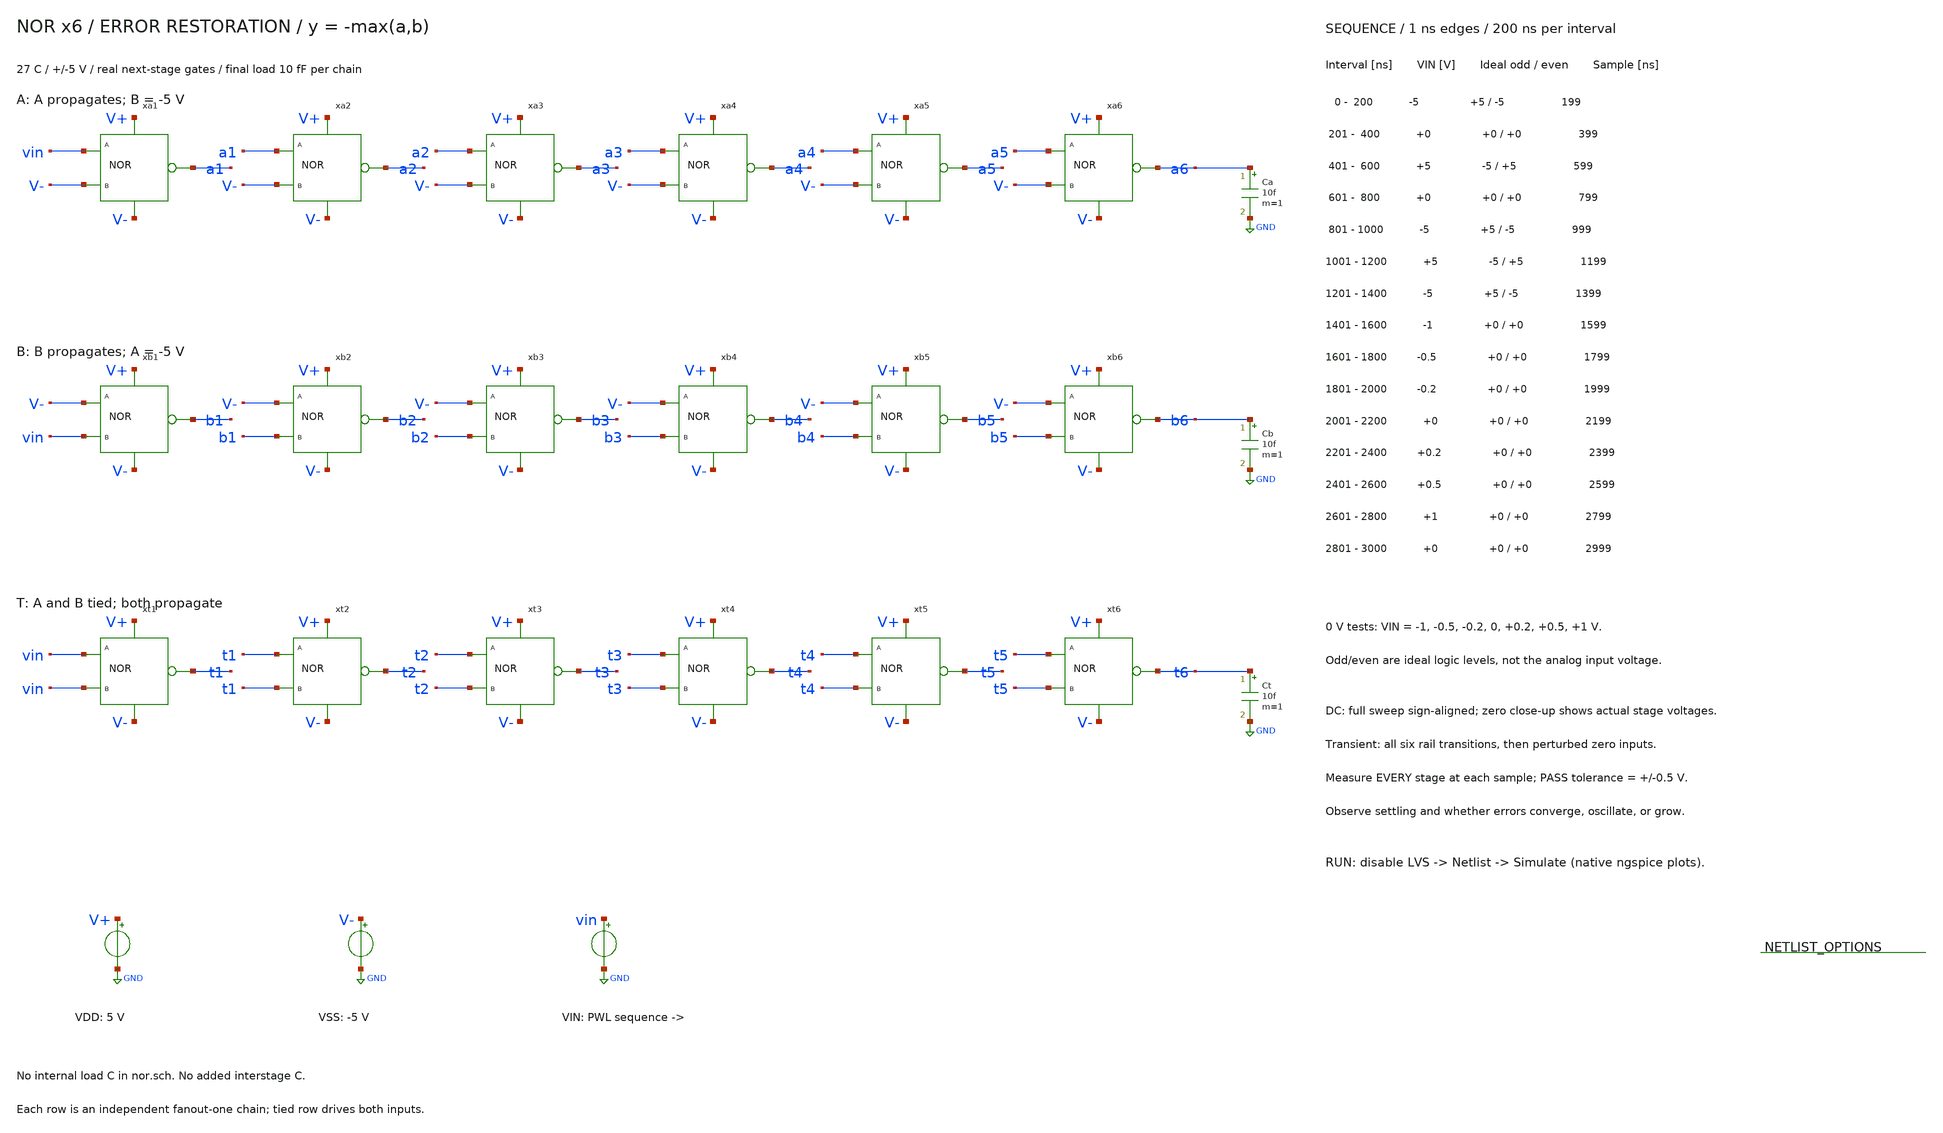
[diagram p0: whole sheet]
** sch_path: member_project/balanced-ternary-logic/PenguinEino/nor_chain_tb.sch
**.subckt nor_chain_tb
xa1 vin V- a1 V+ V- nor
xa2 a1 V- a2 V+ V- nor
xa3 a2 V- a3 V+ V- nor
xa4 a3 V- a4 V+ V- nor
xa5 a4 V- a5 V+ V- nor
xa6 a5 V- a6 V+ V- nor
Ca a6 GND 10f m=1
xb1 V- vin b1 V+ V- nor
xb2 V- b1 b2 V+ V- nor
xb3 V- b2 b3 V+ V- nor
xb4 V- b3 b4 V+ V- nor
xb5 V- b4 b5 V+ V- nor
xb6 V- b5 b6 V+ V- nor
Cb b6 GND 10f m=1
xt1 vin vin t1 V+ V- nor
xt2 t1 t1 t2 V+ V- nor
xt3 t2 t2 t3 V+ V- nor
xt4 t3 t3 t4 V+ V- nor
xt5 t4 t4 t5 V+ V- nor
xt6 t5 t5 t6 V+ V- nor
Ct t6 GND 10f m=1
VDD V+ GND 5
VSS V- GND -5
VIN vin GND PWL(0 -5 200n -5 201n 0 400n 0 401n 5 600n 5 601n 0 800n 0 801n -5 1000n -5 1001n 5
+ 1200n 5 1201n -5 1400n -5 1401n -1 1600n -1 1601n -0.5 1800n -0.5 1801n -0.2 2000n -0.2 2001n 0 2200n 0
+ 2201n 0.2 2400n 0.2 2401n 0.5 2600n 0.5 2601n 1 2800n 1 2801n 0 3000n 0)
**** begin user architecture code
 .include $::LIB/ip62_models

.temp 27
.options rshunt=1e12
.control
save all
set wr_singlescale
set wr_vecnames
setplot const
let failures=0
dc VIN -5 5 0.025
let as1=-v(a1)
let as2=v(a2)
let as3=-v(a3)
let as4=v(a4)
let as5=-v(a5)
let as6=v(a6)
plot v(vin) as1 as2 as3 as4 as5 as6 ylimit -5.5 5.5 title 'NOR a: DC sign-aligned stages'
plot v(vin) v(a1) v(a2) v(a3) v(a4) v(a5) v(a6) xlimit -1 1 ylimit -0.7 0.7 title 'NOR a: zero restoration actual voltages'
let bs1=-v(b1)
let bs2=v(b2)
let bs3=-v(b3)
let bs4=v(b4)
let bs5=-v(b5)
let bs6=v(b6)
plot v(vin) bs1 bs2 bs3 bs4 bs5 bs6 ylimit -5.5 5.5 title 'NOR b: DC sign-aligned stages'
plot v(vin) v(b1) v(b2) v(b3) v(b4) v(b5) v(b6) xlimit -1 1 ylimit -0.7 0.7 title 'NOR b: zero restoration actual voltages'
let ts1=-v(t1)
let ts2=v(t2)
let ts3=-v(t3)
let ts4=v(t4)
let ts5=-v(t5)
let ts6=v(t6)
plot v(vin) ts1 ts2 ts3 ts4 ts5 ts6 ylimit -5.5 5.5 title 'NOR t: DC sign-aligned stages'
plot v(vin) v(t1) v(t2) v(t3) v(t4) v(t5) v(t6) xlimit -1 1 ylimit -0.7 0.7 title 'NOR t: zero restoration actual voltages'
wrdata nor_chain_dc.txt v(vin) v(a1) v(a2) v(a3) v(a4) v(a5) v(a6) v(b1) v(b2) v(b3) v(b4) v(b5)
+ v(b6) v(t1) v(t2) v(t3) v(t4) v(t5) v(t6)
reset
tran 0.2n 3000n
plot v(vin) v(a1) v(a2) v(a3) v(a4) v(a5) v(a6) title 'NOR a: all six stages'
plot v(vin) v(a1) v(a2) v(a3) v(a4) v(a5) v(a6) xlimit 1.4u 3u ylimit -1.1 1.1 title 'NOR a: perturbed zero propagation'
plot v(vin) v(b1) v(b2) v(b3) v(b4) v(b5) v(b6) title 'NOR b: all six stages'
plot v(vin) v(b1) v(b2) v(b3) v(b4) v(b5) v(b6) xlimit 1.4u 3u ylimit -1.1 1.1 title 'NOR b: perturbed zero propagation'
plot v(vin) v(t1) v(t2) v(t3) v(t4) v(t5) v(t6) title 'NOR t: all six stages'
plot v(vin) v(t1) v(t2) v(t3) v(t4) v(t5) v(t6) xlimit 1.4u 3u ylimit -1.1 1.1 title 'NOR t: perturbed zero propagation'
wrdata nor_chain_tran.txt v(vin) v(a1) v(a2) v(a3) v(a4) v(a5) v(a6) v(b1) v(b2) v(b3) v(b4) v(b5)
+ v(b6) v(t1) v(t2) v(t3) v(t4) v(t5) v(t6)
meas tran a1_sample01 find v(a1) at=199n
if abs(a1_sample01-(5)) > 0.5
let const.failures=const.failures+1
echo FAIL: a1_sample01 expected 5 V
end
meas tran a2_sample01 find v(a2) at=199n
if abs(a2_sample01-(-5)) > 0.5
let const.failures=const.failures+1
echo FAIL: a2_sample01 expected -5 V
end
meas tran a3_sample01 find v(a3) at=199n
if abs(a3_sample01-(5)) > 0.5
let const.failures=const.failures+1
echo FAIL: a3_sample01 expected 5 V
end
meas tran a4_sample01 find v(a4) at=199n
if abs(a4_sample01-(-5)) > 0.5
let const.failures=const.failures+1
echo FAIL: a4_sample01 expected -5 V
end
meas tran a5_sample01 find v(a5) at=199n
if abs(a5_sample01-(5)) > 0.5
let const.failures=const.failures+1
echo FAIL: a5_sample01 expected 5 V
end
meas tran a6_sample01 find v(a6) at=199n
if abs(a6_sample01-(-5)) > 0.5
let const.failures=const.failures+1
echo FAIL: a6_sample01 expected -5 V
end
meas tran b1_sample01 find v(b1) at=199n
if abs(b1_sample01-(5)) > 0.5
let const.failures=const.failures+1
echo FAIL: b1_sample01 expected 5 V
end
meas tran b2_sample01 find v(b2) at=199n
if abs(b2_sample01-(-5)) > 0.5
let const.failures=const.failures+1
echo FAIL: b2_sample01 expected -5 V
end
meas tran b3_sample01 find v(b3) at=199n
if abs(b3_sample01-(5)) > 0.5
let const.failures=const.failures+1
echo FAIL: b3_sample01 expected 5 V
end
meas tran b4_sample01 find v(b4) at=199n
if abs(b4_sample01-(-5)) > 0.5
let const.failures=const.failures+1
echo FAIL: b4_sample01 expected -5 V
end
meas tran b5_sample01 find v(b5) at=199n
if abs(b5_sample01-(5)) > 0.5
let const.failures=const.failures+1
echo FAIL: b5_sample01 expected 5 V
end
meas tran b6_sample01 find v(b6) at=199n
if abs(b6_sample01-(-5)) > 0.5
let const.failures=const.failures+1
echo FAIL: b6_sample01 expected -5 V
end
meas tran t1_sample01 find v(t1) at=199n
if abs(t1_sample01-(5)) > 0.5
let const.failures=const.failures+1
echo FAIL: t1_sample01 expected 5 V
end
meas tran t2_sample01 find v(t2) at=199n
if abs(t2_sample01-(-5)) > 0.5
let const.failures=const.failures+1
echo FAIL: t2_sample01 expected -5 V
end
meas tran t3_sample01 find v(t3) at=199n
if abs(t3_sample01-(5)) > 0.5
let const.failures=const.failures+1
echo FAIL: t3_sample01 expected 5 V
end
meas tran t4_sample01 find v(t4) at=199n
if abs(t4_sample01-(-5)) > 0.5
let const.failures=const.failures+1
echo FAIL: t4_sample01 expected -5 V
end
meas tran t5_sample01 find v(t5) at=199n
if abs(t5_sample01-(5)) > 0.5
let const.failures=const.failures+1
echo FAIL: t5_sample01 expected 5 V
end
meas tran t6_sample01 find v(t6) at=199n
if abs(t6_sample01-(-5)) > 0.5
let const.failures=const.failures+1
echo FAIL: t6_sample01 expected -5 V
end
meas tran a1_sample02 find v(a1) at=399n
if abs(a1_sample02-(0)) > 0.5
let const.failures=const.failures+1
echo FAIL: a1_sample02 expected 0 V
end
meas tran a2_sample02 find v(a2) at=399n
if abs(a2_sample02-(0)) > 0.5
let const.failures=const.failures+1
echo FAIL: a2_sample02 expected 0 V
end
meas tran a3_sample02 find v(a3) at=399n
if abs(a3_sample02-(0)) > 0.5
let const.failures=const.failures+1
echo FAIL: a3_sample02 expected 0 V
end
meas tran a4_sample02 find v(a4) at=399n
if abs(a4_sample02-(0)) > 0.5
let const.failures=const.failures+1
echo FAIL: a4_sample02 expected 0 V
end
meas tran a5_sample02 find v(a5) at=399n
if abs(a5_sample02-(0)) > 0.5
let const.failures=const.failures+1
echo FAIL: a5_sample02 expected 0 V
end
meas tran a6_sample02 find v(a6) at=399n
if abs(a6_sample02-(0)) > 0.5
let const.failures=const.failures+1
echo FAIL: a6_sample02 expected 0 V
end
meas tran b1_sample02 find v(b1) at=399n
if abs(b1_sample02-(0)) > 0.5
let const.failures=const.failures+1
echo FAIL: b1_sample02 expected 0 V
end
meas tran b2_sample02 find v(b2) at=399n
if abs(b2_sample02-(0)) > 0.5
let const.failures=const.failures+1
echo FAIL: b2_sample02 expected 0 V
end
meas tran b3_sample02 find v(b3) at=399n
if abs(b3_sample02-(0)) > 0.5
let const.failures=const.failures+1
echo FAIL: b3_sample02 expected 0 V
end
meas tran b4_sample02 find v(b4) at=399n
if abs(b4_sample02-(0)) > 0.5
let const.failures=const.failures+1
echo FAIL: b4_sample02 expected 0 V
end
meas tran b5_sample02 find v(b5) at=399n
if abs(b5_sample02-(0)) > 0.5
let const.failures=const.failures+1
echo FAIL: b5_sample02 expected 0 V
end
meas tran b6_sample02 find v(b6) at=399n
if abs(b6_sample02-(0)) > 0.5
let const.failures=const.failures+1
echo FAIL: b6_sample02 expected 0 V
end
meas tran t1_sample02 find v(t1) at=399n
if abs(t1_sample02-(0)) > 0.5
let const.failures=const.failures+1
echo FAIL: t1_sample02 expected 0 V
end
meas tran t2_sample02 find v(t2) at=399n
if abs(t2_sample02-(0)) > 0.5
let const.failures=const.failures+1
echo FAIL: t2_sample02 expected 0 V
end
meas tran t3_sample02 find v(t3) at=399n
if abs(t3_sample02-(0)) > 0.5
let const.failures=const.failures+1
echo FAIL: t3_sample02 expected 0 V
end
meas tran t4_sample02 find v(t4) at=399n
if abs(t4_sample02-(0)) > 0.5
let const.failures=const.failures+1
echo FAIL: t4_sample02 expected 0 V
end
meas tran t5_sample02 find v(t5) at=399n
if abs(t5_sample02-(0)) > 0.5
let const.failures=const.failures+1
echo FAIL: t5_sample02 expected 0 V
end
meas tran t6_sample02 find v(t6) at=399n
if abs(t6_sample02-(0)) > 0.5
let const.failures=const.failures+1
echo FAIL: t6_sample02 expected 0 V
end
meas tran a1_sample03 find v(a1) at=599n
if abs(a1_sample03-(-5)) > 0.5
let const.failures=const.failures+1
echo FAIL: a1_sample03 expected -5 V
end
meas tran a2_sample03 find v(a2) at=599n
if abs(a2_sample03-(5)) > 0.5
let const.failures=const.failures+1
echo FAIL: a2_sample03 expected 5 V
end
meas tran a3_sample03 find v(a3) at=599n
if abs(a3_sample03-(-5)) > 0.5
let const.failures=const.failures+1
echo FAIL: a3_sample03 expected -5 V
end
meas tran a4_sample03 find v(a4) at=599n
if abs(a4_sample03-(5)) > 0.5
let const.failures=const.failures+1
echo FAIL: a4_sample03 expected 5 V
end
meas tran a5_sample03 find v(a5) at=599n
if abs(a5_sample03-(-5)) > 0.5
let const.failures=const.failures+1
echo FAIL: a5_sample03 expected -5 V
end
meas tran a6_sample03 find v(a6) at=599n
if abs(a6_sample03-(5)) > 0.5
let const.failures=const.failures+1
echo FAIL: a6_sample03 expected 5 V
end
meas tran b1_sample03 find v(b1) at=599n
if abs(b1_sample03-(-5)) > 0.5
let const.failures=const.failures+1
echo FAIL: b1_sample03 expected -5 V
end
meas tran b2_sample03 find v(b2) at=599n
if abs(b2_sample03-(5)) > 0.5
let const.failures=const.failures+1
echo FAIL: b2_sample03 expected 5 V
end
meas tran b3_sample03 find v(b3) at=599n
if abs(b3_sample03-(-5)) > 0.5
let const.failures=const.failures+1
echo FAIL: b3_sample03 expected -5 V
end
meas tran b4_sample03 find v(b4) at=599n
if abs(b4_sample03-(5)) > 0.5
let const.failures=const.failures+1
echo FAIL: b4_sample03 expected 5 V
end
meas tran b5_sample03 find v(b5) at=599n
if abs(b5_sample03-(-5)) > 0.5
let const.failures=const.failures+1
echo FAIL: b5_sample03 expected -5 V
end
meas tran b6_sample03 find v(b6) at=599n
if abs(b6_sample03-(5)) > 0.5
let const.failures=const.failures+1
echo FAIL: b6_sample03 expected 5 V
end
meas tran t1_sample03 find v(t1) at=599n
if abs(t1_sample03-(-5)) > 0.5
let const.failures=const.failures+1
echo FAIL: t1_sample03 expected -5 V
end
meas tran t2_sample03 find v(t2) at=599n
if abs(t2_sample03-(5)) > 0.5
let const.failures=const.failures+1
echo FAIL: t2_sample03 expected 5 V
end
meas tran t3_sample03 find v(t3) at=599n
if abs(t3_sample03-(-5)) > 0.5
let const.failures=const.failures+1
echo FAIL: t3_sample03 expected -5 V
end
meas tran t4_sample03 find v(t4) at=599n
if abs(t4_sample03-(5)) > 0.5
let const.failures=const.failures+1
echo FAIL: t4_sample03 expected 5 V
end
meas tran t5_sample03 find v(t5) at=599n
if abs(t5_sample03-(-5)) > 0.5
let const.failures=const.failures+1
echo FAIL: t5_sample03 expected -5 V
end
meas tran t6_sample03 find v(t6) at=599n
if abs(t6_sample03-(5)) > 0.5
let const.failures=const.failures+1
echo FAIL: t6_sample03 expected 5 V
end
meas tran a1_sample04 find v(a1) at=799n
if abs(a1_sample04-(0)) > 0.5
let const.failures=const.failures+1
echo FAIL: a1_sample04 expected 0 V
end
meas tran a2_sample04 find v(a2) at=799n
if abs(a2_sample04-(0)) > 0.5
let const.failures=const.failures+1
echo FAIL: a2_sample04 expected 0 V
end
meas tran a3_sample04 find v(a3) at=799n
if abs(a3_sample04-(0)) > 0.5
let const.failures=const.failures+1
echo FAIL: a3_sample04 expected 0 V
end
meas tran a4_sample04 find v(a4) at=799n
if abs(a4_sample04-(0)) > 0.5
let const.failures=const.failures+1
echo FAIL: a4_sample04 expected 0 V
end
meas tran a5_sample04 find v(a5) at=799n
if abs(a5_sample04-(0)) > 0.5
let const.failures=const.failures+1
echo FAIL: a5_sample04 expected 0 V
end
meas tran a6_sample04 find v(a6) at=799n
if abs(a6_sample04-(0)) > 0.5
let const.failures=const.failures+1
echo FAIL: a6_sample04 expected 0 V
end
meas tran b1_sample04 find v(b1) at=799n
if abs(b1_sample04-(0)) > 0.5
let const.failures=const.failures+1
echo FAIL: b1_sample04 expected 0 V
end
meas tran b2_sample04 find v(b2) at=799n
if abs(b2_sample04-(0)) > 0.5
let const.failures=const.failures+1
echo FAIL: b2_sample04 expected 0 V
end
meas tran b3_sample04 find v(b3) at=799n
if abs(b3_sample04-(0)) > 0.5
let const.failures=const.failures+1
echo FAIL: b3_sample04 expected 0 V
end
meas tran b4_sample04 find v(b4) at=799n
if abs(b4_sample04-(0)) > 0.5
let const.failures=const.failures+1
echo FAIL: b4_sample04 expected 0 V
end
meas tran b5_sample04 find v(b5) at=799n
if abs(b5_sample04-(0)) > 0.5
let const.failures=const.failures+1
echo FAIL: b5_sample04 expected 0 V
end
meas tran b6_sample04 find v(b6) at=799n
if abs(b6_sample04-(0)) > 0.5
let const.failures=const.failures+1
echo FAIL: b6_sample04 expected 0 V
end
meas tran t1_sample04 find v(t1) at=799n
if abs(t1_sample04-(0)) > 0.5
let const.failures=const.failures+1
echo FAIL: t1_sample04 expected 0 V
end
meas tran t2_sample04 find v(t2) at=799n
if abs(t2_sample04-(0)) > 0.5
let const.failures=const.failures+1
echo FAIL: t2_sample04 expected 0 V
end
meas tran t3_sample04 find v(t3) at=799n
if abs(t3_sample04-(0)) > 0.5
let const.failures=const.failures+1
echo FAIL: t3_sample04 expected 0 V
end
meas tran t4_sample04 find v(t4) at=799n
if abs(t4_sample04-(0)) > 0.5
let const.failures=const.failures+1
echo FAIL: t4_sample04 expected 0 V
end
meas tran t5_sample04 find v(t5) at=799n
if abs(t5_sample04-(0)) > 0.5
let const.failures=const.failures+1
echo FAIL: t5_sample04 expected 0 V
end
meas tran t6_sample04 find v(t6) at=799n
if abs(t6_sample04-(0)) > 0.5
let const.failures=const.failures+1
echo FAIL: t6_sample04 expected 0 V
end
meas tran a1_sample05 find v(a1) at=999n
if abs(a1_sample05-(5)) > 0.5
let const.failures=const.failures+1
echo FAIL: a1_sample05 expected 5 V
end
meas tran a2_sample05 find v(a2) at=999n
if abs(a2_sample05-(-5)) > 0.5
let const.failures=const.failures+1
echo FAIL: a2_sample05 expected -5 V
end
meas tran a3_sample05 find v(a3) at=999n
if abs(a3_sample05-(5)) > 0.5
let const.failures=const.failures+1
echo FAIL: a3_sample05 expected 5 V
end
meas tran a4_sample05 find v(a4) at=999n
if abs(a4_sample05-(-5)) > 0.5
let const.failures=const.failures+1
echo FAIL: a4_sample05 expected -5 V
end
meas tran a5_sample05 find v(a5) at=999n
if abs(a5_sample05-(5)) > 0.5
let const.failures=const.failures+1
echo FAIL: a5_sample05 expected 5 V
end
meas tran a6_sample05 find v(a6) at=999n
if abs(a6_sample05-(-5)) > 0.5
let const.failures=const.failures+1
echo FAIL: a6_sample05 expected -5 V
end
meas tran b1_sample05 find v(b1) at=999n
if abs(b1_sample05-(5)) > 0.5
let const.failures=const.failures+1
echo FAIL: b1_sample05 expected 5 V
end
meas tran b2_sample05 find v(b2) at=999n
if abs(b2_sample05-(-5)) > 0.5
let const.failures=const.failures+1
echo FAIL: b2_sample05 expected -5 V
end
meas tran b3_sample05 find v(b3) at=999n
if abs(b3_sample05-(5)) > 0.5
let const.failures=const.failures+1
echo FAIL: b3_sample05 expected 5 V
end
meas tran b4_sample05 find v(b4) at=999n
if abs(b4_sample05-(-5)) > 0.5
let const.failures=const.failures+1
echo FAIL: b4_sample05 expected -5 V
end
meas tran b5_sample05 find v(b5) at=999n
if abs(b5_sample05-(5)) > 0.5
let const.failures=const.failures+1
echo FAIL: b5_sample05 expected 5 V
end
meas tran b6_sample05 find v(b6) at=999n
if abs(b6_sample05-(-5)) > 0.5
let const.failures=const.failures+1
echo FAIL: b6_sample05 expected -5 V
end
meas tran t1_sample05 find v(t1) at=999n
if abs(t1_sample05-(5)) > 0.5
let const.failures=const.failures+1
echo FAIL: t1_sample05 expected 5 V
end
meas tran t2_sample05 find v(t2) at=999n
if abs(t2_sample05-(-5)) > 0.5
let const.failures=const.failures+1
echo FAIL: t2_sample05 expected -5 V
end
meas tran t3_sample05 find v(t3) at=999n
if abs(t3_sample05-(5)) > 0.5
let const.failures=const.failures+1
echo FAIL: t3_sample05 expected 5 V
end
meas tran t4_sample05 find v(t4) at=999n
if abs(t4_sample05-(-5)) > 0.5
let const.failures=const.failures+1
echo FAIL: t4_sample05 expected -5 V
end
meas tran t5_sample05 find v(t5) at=999n
if abs(t5_sample05-(5)) > 0.5
let const.failures=const.failures+1
echo FAIL: t5_sample05 expected 5 V
end
meas tran t6_sample05 find v(t6) at=999n
if abs(t6_sample05-(-5)) > 0.5
let const.failures=const.failures+1
echo FAIL: t6_sample05 expected -5 V
end
meas tran a1_sample06 find v(a1) at=1199n
if abs(a1_sample06-(-5)) > 0.5
let const.failures=const.failures+1
echo FAIL: a1_sample06 expected -5 V
end
meas tran a2_sample06 find v(a2) at=1199n
if abs(a2_sample06-(5)) > 0.5
let const.failures=const.failures+1
echo FAIL: a2_sample06 expected 5 V
end
meas tran a3_sample06 find v(a3) at=1199n
if abs(a3_sample06-(-5)) > 0.5
let const.failures=const.failures+1
echo FAIL: a3_sample06 expected -5 V
end
meas tran a4_sample06 find v(a4) at=1199n
if abs(a4_sample06-(5)) > 0.5
let const.failures=const.failures+1
echo FAIL: a4_sample06 expected 5 V
end
meas tran a5_sample06 find v(a5) at=1199n
if abs(a5_sample06-(-5)) > 0.5
let const.failures=const.failures+1
echo FAIL: a5_sample06 expected -5 V
end
meas tran a6_sample06 find v(a6) at=1199n
if abs(a6_sample06-(5)) > 0.5
let const.failures=const.failures+1
echo FAIL: a6_sample06 expected 5 V
end
meas tran b1_sample06 find v(b1) at=1199n
if abs(b1_sample06-(-5)) > 0.5
let const.failures=const.failures+1
echo FAIL: b1_sample06 expected -5 V
end
meas tran b2_sample06 find v(b2) at=1199n
if abs(b2_sample06-(5)) > 0.5
let const.failures=const.failures+1
echo FAIL: b2_sample06 expected 5 V
end
meas tran b3_sample06 find v(b3) at=1199n
if abs(b3_sample06-(-5)) > 0.5
let const.failures=const.failures+1
echo FAIL: b3_sample06 expected -5 V
end
meas tran b4_sample06 find v(b4) at=1199n
if abs(b4_sample06-(5)) > 0.5
let const.failures=const.failures+1
echo FAIL: b4_sample06 expected 5 V
end
meas tran b5_sample06 find v(b5) at=1199n
if abs(b5_sample06-(-5)) > 0.5
let const.failures=const.failures+1
echo FAIL: b5_sample06 expected -5 V
end
meas tran b6_sample06 find v(b6) at=1199n
if abs(b6_sample06-(5)) > 0.5
let const.failures=const.failures+1
echo FAIL: b6_sample06 expected 5 V
end
meas tran t1_sample06 find v(t1) at=1199n
if abs(t1_sample06-(-5)) > 0.5
let const.failures=const.failures+1
echo FAIL: t1_sample06 expected -5 V
end
meas tran t2_sample06 find v(t2) at=1199n
if abs(t2_sample06-(5)) > 0.5
let const.failures=const.failures+1
echo FAIL: t2_sample06 expected 5 V
end
meas tran t3_sample06 find v(t3) at=1199n
if abs(t3_sample06-(-5)) > 0.5
let const.failures=const.failures+1
echo FAIL: t3_sample06 expected -5 V
end
meas tran t4_sample06 find v(t4) at=1199n
if abs(t4_sample06-(5)) > 0.5
let const.failures=const.failures+1
echo FAIL: t4_sample06 expected 5 V
end
meas tran t5_sample06 find v(t5) at=1199n
if abs(t5_sample06-(-5)) > 0.5
let const.failures=const.failures+1
echo FAIL: t5_sample06 expected -5 V
end
meas tran t6_sample06 find v(t6) at=1199n
if abs(t6_sample06-(5)) > 0.5
let const.failures=const.failures+1
echo FAIL: t6_sample06 expected 5 V
end
meas tran a1_sample07 find v(a1) at=1399n
if abs(a1_sample07-(5)) > 0.5
let const.failures=const.failures+1
echo FAIL: a1_sample07 expected 5 V
end
meas tran a2_sample07 find v(a2) at=1399n
if abs(a2_sample07-(-5)) > 0.5
let const.failures=const.failures+1
echo FAIL: a2_sample07 expected -5 V
end
meas tran a3_sample07 find v(a3) at=1399n
if abs(a3_sample07-(5)) > 0.5
let const.failures=const.failures+1
echo FAIL: a3_sample07 expected 5 V
end
meas tran a4_sample07 find v(a4) at=1399n
if abs(a4_sample07-(-5)) > 0.5
let const.failures=const.failures+1
echo FAIL: a4_sample07 expected -5 V
end
meas tran a5_sample07 find v(a5) at=1399n
if abs(a5_sample07-(5)) > 0.5
let const.failures=const.failures+1
echo FAIL: a5_sample07 expected 5 V
end
meas tran a6_sample07 find v(a6) at=1399n
if abs(a6_sample07-(-5)) > 0.5
let const.failures=const.failures+1
echo FAIL: a6_sample07 expected -5 V
end
meas tran b1_sample07 find v(b1) at=1399n
if abs(b1_sample07-(5)) > 0.5
let const.failures=const.failures+1
echo FAIL: b1_sample07 expected 5 V
end
meas tran b2_sample07 find v(b2) at=1399n
if abs(b2_sample07-(-5)) > 0.5
let const.failures=const.failures+1
echo FAIL: b2_sample07 expected -5 V
end
meas tran b3_sample07 find v(b3) at=1399n
if abs(b3_sample07-(5)) > 0.5
let const.failures=const.failures+1
echo FAIL: b3_sample07 expected 5 V
end
meas tran b4_sample07 find v(b4) at=1399n
if abs(b4_sample07-(-5)) > 0.5
let const.failures=const.failures+1
echo FAIL: b4_sample07 expected -5 V
end
meas tran b5_sample07 find v(b5) at=1399n
if abs(b5_sample07-(5)) > 0.5
let const.failures=const.failures+1
echo FAIL: b5_sample07 expected 5 V
end
meas tran b6_sample07 find v(b6) at=1399n
if abs(b6_sample07-(-5)) > 0.5
let const.failures=const.failures+1
echo FAIL: b6_sample07 expected -5 V
end
meas tran t1_sample07 find v(t1) at=1399n
if abs(t1_sample07-(5)) > 0.5
let const.failures=const.failures+1
echo FAIL: t1_sample07 expected 5 V
end
meas tran t2_sample07 find v(t2) at=1399n
if abs(t2_sample07-(-5)) > 0.5
let const.failures=const.failures+1
echo FAIL: t2_sample07 expected -5 V
end
meas tran t3_sample07 find v(t3) at=1399n
if abs(t3_sample07-(5)) > 0.5
let const.failures=const.failures+1
echo FAIL: t3_sample07 expected 5 V
end
meas tran t4_sample07 find v(t4) at=1399n
if abs(t4_sample07-(-5)) > 0.5
let const.failures=const.failures+1
echo FAIL: t4_sample07 expected -5 V
end
meas tran t5_sample07 find v(t5) at=1399n
if abs(t5_sample07-(5)) > 0.5
let const.failures=const.failures+1
echo FAIL: t5_sample07 expected 5 V
end
meas tran t6_sample07 find v(t6) at=1399n
if abs(t6_sample07-(-5)) > 0.5
let const.failures=const.failures+1
echo FAIL: t6_sample07 expected -5 V
end
meas tran a1_sample08 find v(a1) at=1599n
if abs(a1_sample08-(0)) > 0.5
let const.failures=const.failures+1
echo FAIL: a1_sample08 expected 0 V
end
meas tran a2_sample08 find v(a2) at=1599n
if abs(a2_sample08-(0)) > 0.5
let const.failures=const.failures+1
echo FAIL: a2_sample08 expected 0 V
end
meas tran a3_sample08 find v(a3) at=1599n
if abs(a3_sample08-(0)) > 0.5
let const.failures=const.failures+1
echo FAIL: a3_sample08 expected 0 V
end
meas tran a4_sample08 find v(a4) at=1599n
if abs(a4_sample08-(0)) > 0.5
let const.failures=const.failures+1
echo FAIL: a4_sample08 expected 0 V
end
meas tran a5_sample08 find v(a5) at=1599n
if abs(a5_sample08-(0)) > 0.5
let const.failures=const.failures+1
echo FAIL: a5_sample08 expected 0 V
end
meas tran a6_sample08 find v(a6) at=1599n
if abs(a6_sample08-(0)) > 0.5
let const.failures=const.failures+1
echo FAIL: a6_sample08 expected 0 V
end
meas tran b1_sample08 find v(b1) at=1599n
if abs(b1_sample08-(0)) > 0.5
let const.failures=const.failures+1
echo FAIL: b1_sample08 expected 0 V
end
meas tran b2_sample08 find v(b2) at=1599n
if abs(b2_sample08-(0)) > 0.5
let const.failures=const.failures+1
echo FAIL: b2_sample08 expected 0 V
end
meas tran b3_sample08 find v(b3) at=1599n
if abs(b3_sample08-(0)) > 0.5
let const.failures=const.failures+1
echo FAIL: b3_sample08 expected 0 V
end
meas tran b4_sample08 find v(b4) at=1599n
if abs(b4_sample08-(0)) > 0.5
let const.failures=const.failures+1
echo FAIL: b4_sample08 expected 0 V
end
meas tran b5_sample08 find v(b5) at=1599n
if abs(b5_sample08-(0)) > 0.5
let const.failures=const.failures+1
echo FAIL: b5_sample08 expected 0 V
end
meas tran b6_sample08 find v(b6) at=1599n
if abs(b6_sample08-(0)) > 0.5
let const.failures=const.failures+1
echo FAIL: b6_sample08 expected 0 V
end
meas tran t1_sample08 find v(t1) at=1599n
if abs(t1_sample08-(0)) > 0.5
let const.failures=const.failures+1
echo FAIL: t1_sample08 expected 0 V
end
meas tran t2_sample08 find v(t2) at=1599n
if abs(t2_sample08-(0)) > 0.5
let const.failures=const.failures+1
echo FAIL: t2_sample08 expected 0 V
end
meas tran t3_sample08 find v(t3) at=1599n
if abs(t3_sample08-(0)) > 0.5
let const.failures=const.failures+1
echo FAIL: t3_sample08 expected 0 V
end
meas tran t4_sample08 find v(t4) at=1599n
if abs(t4_sample08-(0)) > 0.5
let const.failures=const.failures+1
echo FAIL: t4_sample08 expected 0 V
end
meas tran t5_sample08 find v(t5) at=1599n
if abs(t5_sample08-(0)) > 0.5
let const.failures=const.failures+1
echo FAIL: t5_sample08 expected 0 V
end
meas tran t6_sample08 find v(t6) at=1599n
if abs(t6_sample08-(0)) > 0.5
let const.failures=const.failures+1
echo FAIL: t6_sample08 expected 0 V
end
meas tran a1_sample09 find v(a1) at=1799n
if abs(a1_sample09-(0)) > 0.5
let const.failures=const.failures+1
echo FAIL: a1_sample09 expected 0 V
end
meas tran a2_sample09 find v(a2) at=1799n
if abs(a2_sample09-(0)) > 0.5
let const.failures=const.failures+1
echo FAIL: a2_sample09 expected 0 V
end
meas tran a3_sample09 find v(a3) at=1799n
if abs(a3_sample09-(0)) > 0.5
let const.failures=const.failures+1
echo FAIL: a3_sample09 expected 0 V
end
meas tran a4_sample09 find v(a4) at=1799n
if abs(a4_sample09-(0)) > 0.5
let const.failures=const.failures+1
echo FAIL: a4_sample09 expected 0 V
end
meas tran a5_sample09 find v(a5) at=1799n
if abs(a5_sample09-(0)) > 0.5
let const.failures=const.failures+1
echo FAIL: a5_sample09 expected 0 V
end
meas tran a6_sample09 find v(a6) at=1799n
if abs(a6_sample09-(0)) > 0.5
let const.failures=const.failures+1
echo FAIL: a6_sample09 expected 0 V
end
meas tran b1_sample09 find v(b1) at=1799n
if abs(b1_sample09-(0)) > 0.5
let const.failures=const.failures+1
echo FAIL: b1_sample09 expected 0 V
end
meas tran b2_sample09 find v(b2) at=1799n
if abs(b2_sample09-(0)) > 0.5
let const.failures=const.failures+1
echo FAIL: b2_sample09 expected 0 V
end
meas tran b3_sample09 find v(b3) at=1799n
if abs(b3_sample09-(0)) > 0.5
let const.failures=const.failures+1
echo FAIL: b3_sample09 expected 0 V
end
meas tran b4_sample09 find v(b4) at=1799n
if abs(b4_sample09-(0)) > 0.5
let const.failures=const.failures+1
echo FAIL: b4_sample09 expected 0 V
end
meas tran b5_sample09 find v(b5) at=1799n
if abs(b5_sample09-(0)) > 0.5
let const.failures=const.failures+1
echo FAIL: b5_sample09 expected 0 V
end
meas tran b6_sample09 find v(b6) at=1799n
if abs(b6_sample09-(0)) > 0.5
let const.failures=const.failures+1
echo FAIL: b6_sample09 expected 0 V
end
meas tran t1_sample09 find v(t1) at=1799n
if abs(t1_sample09-(0)) > 0.5
let const.failures=const.failures+1
echo FAIL: t1_sample09 expected 0 V
end
meas tran t2_sample09 find v(t2) at=1799n
if abs(t2_sample09-(0)) > 0.5
let const.failures=const.failures+1
echo FAIL: t2_sample09 expected 0 V
end
meas tran t3_sample09 find v(t3) at=1799n
if abs(t3_sample09-(0)) > 0.5
let const.failures=const.failures+1
echo FAIL: t3_sample09 expected 0 V
end
meas tran t4_sample09 find v(t4) at=1799n
if abs(t4_sample09-(0)) > 0.5
let const.failures=const.failures+1
echo FAIL: t4_sample09 expected 0 V
end
meas tran t5_sample09 find v(t5) at=1799n
if abs(t5_sample09-(0)) > 0.5
let const.failures=const.failures+1
echo FAIL: t5_sample09 expected 0 V
end
meas tran t6_sample09 find v(t6) at=1799n
if abs(t6_sample09-(0)) > 0.5
let const.failures=const.failures+1
echo FAIL: t6_sample09 expected 0 V
end
meas tran a1_sample10 find v(a1) at=1999n
if abs(a1_sample10-(0)) > 0.5
let const.failures=const.failures+1
echo FAIL: a1_sample10 expected 0 V
end
meas tran a2_sample10 find v(a2) at=1999n
if abs(a2_sample10-(0)) > 0.5
let const.failures=const.failures+1
echo FAIL: a2_sample10 expected 0 V
end
meas tran a3_sample10 find v(a3) at=1999n
if abs(a3_sample10-(0)) > 0.5
let const.failures=const.failures+1
echo FAIL: a3_sample10 expected 0 V
end
meas tran a4_sample10 find v(a4) at=1999n
if abs(a4_sample10-(0)) > 0.5
let const.failures=const.failures+1
echo FAIL: a4_sample10 expected 0 V
end
meas tran a5_sample10 find v(a5) at=1999n
if abs(a5_sample10-(0)) > 0.5
let const.failures=const.failures+1
echo FAIL: a5_sample10 expected 0 V
end
meas tran a6_sample10 find v(a6) at=1999n
if abs(a6_sample10-(0)) > 0.5
let const.failures=const.failures+1
echo FAIL: a6_sample10 expected 0 V
end
meas tran b1_sample10 find v(b1) at=1999n
if abs(b1_sample10-(0)) > 0.5
let const.failures=const.failures+1
echo FAIL: b1_sample10 expected 0 V
end
meas tran b2_sample10 find v(b2) at=1999n
if abs(b2_sample10-(0)) > 0.5
let const.failures=const.failures+1
echo FAIL: b2_sample10 expected 0 V
end
meas tran b3_sample10 find v(b3) at=1999n
if abs(b3_sample10-(0)) > 0.5
let const.failures=const.failures+1
echo FAIL: b3_sample10 expected 0 V
end
meas tran b4_sample10 find v(b4) at=1999n
if abs(b4_sample10-(0)) > 0.5
let const.failures=const.failures+1
echo FAIL: b4_sample10 expected 0 V
end
meas tran b5_sample10 find v(b5) at=1999n
if abs(b5_sample10-(0)) > 0.5
let const.failures=const.failures+1
echo FAIL: b5_sample10 expected 0 V
end
meas tran b6_sample10 find v(b6) at=1999n
if abs(b6_sample10-(0)) > 0.5
let const.failures=const.failures+1
echo FAIL: b6_sample10 expected 0 V
end
meas tran t1_sample10 find v(t1) at=1999n
if abs(t1_sample10-(0)) > 0.5
let const.failures=const.failures+1
echo FAIL: t1_sample10 expected 0 V
end
meas tran t2_sample10 find v(t2) at=1999n
if abs(t2_sample10-(0)) > 0.5
let const.failures=const.failures+1
echo FAIL: t2_sample10 expected 0 V
end
meas tran t3_sample10 find v(t3) at=1999n
if abs(t3_sample10-(0)) > 0.5
let const.failures=const.failures+1
echo FAIL: t3_sample10 expected 0 V
end
meas tran t4_sample10 find v(t4) at=1999n
if abs(t4_sample10-(0)) > 0.5
let const.failures=const.failures+1
echo FAIL: t4_sample10 expected 0 V
end
meas tran t5_sample10 find v(t5) at=1999n
if abs(t5_sample10-(0)) > 0.5
let const.failures=const.failures+1
echo FAIL: t5_sample10 expected 0 V
end
meas tran t6_sample10 find v(t6) at=1999n
if abs(t6_sample10-(0)) > 0.5
let const.failures=const.failures+1
echo FAIL: t6_sample10 expected 0 V
end
meas tran a1_sample11 find v(a1) at=2199n
if abs(a1_sample11-(0)) > 0.5
let const.failures=const.failures+1
echo FAIL: a1_sample11 expected 0 V
end
meas tran a2_sample11 find v(a2) at=2199n
if abs(a2_sample11-(0)) > 0.5
let const.failures=const.failures+1
echo FAIL: a2_sample11 expected 0 V
end
meas tran a3_sample11 find v(a3) at=2199n
if abs(a3_sample11-(0)) > 0.5
let const.failures=const.failures+1
echo FAIL: a3_sample11 expected 0 V
end
meas tran a4_sample11 find v(a4) at=2199n
if abs(a4_sample11-(0)) > 0.5
let const.failures=const.failures+1
echo FAIL: a4_sample11 expected 0 V
end
meas tran a5_sample11 find v(a5) at=2199n
if abs(a5_sample11-(0)) > 0.5
let const.failures=const.failures+1
echo FAIL: a5_sample11 expected 0 V
end
meas tran a6_sample11 find v(a6) at=2199n
if abs(a6_sample11-(0)) > 0.5
let const.failures=const.failures+1
echo FAIL: a6_sample11 expected 0 V
end
meas tran b1_sample11 find v(b1) at=2199n
if abs(b1_sample11-(0)) > 0.5
let const.failures=const.failures+1
echo FAIL: b1_sample11 expected 0 V
end
meas tran b2_sample11 find v(b2) at=2199n
if abs(b2_sample11-(0)) > 0.5
let const.failures=const.failures+1
echo FAIL: b2_sample11 expected 0 V
end
meas tran b3_sample11 find v(b3) at=2199n
if abs(b3_sample11-(0)) > 0.5
let const.failures=const.failures+1
echo FAIL: b3_sample11 expected 0 V
end
meas tran b4_sample11 find v(b4) at=2199n
if abs(b4_sample11-(0)) > 0.5
let const.failures=const.failures+1
echo FAIL: b4_sample11 expected 0 V
end
meas tran b5_sample11 find v(b5) at=2199n
if abs(b5_sample11-(0)) > 0.5
let const.failures=const.failures+1
echo FAIL: b5_sample11 expected 0 V
end
meas tran b6_sample11 find v(b6) at=2199n
if abs(b6_sample11-(0)) > 0.5
let const.failures=const.failures+1
echo FAIL: b6_sample11 expected 0 V
end
meas tran t1_sample11 find v(t1) at=2199n
if abs(t1_sample11-(0)) > 0.5
let const.failures=const.failures+1
echo FAIL: t1_sample11 expected 0 V
end
meas tran t2_sample11 find v(t2) at=2199n
if abs(t2_sample11-(0)) > 0.5
let const.failures=const.failures+1
echo FAIL: t2_sample11 expected 0 V
end
meas tran t3_sample11 find v(t3) at=2199n
if abs(t3_sample11-(0)) > 0.5
let const.failures=const.failures+1
echo FAIL: t3_sample11 expected 0 V
end
meas tran t4_sample11 find v(t4) at=2199n
if abs(t4_sample11-(0)) > 0.5
let const.failures=const.failures+1
echo FAIL: t4_sample11 expected 0 V
end
meas tran t5_sample11 find v(t5) at=2199n
if abs(t5_sample11-(0)) > 0.5
let const.failures=const.failures+1
echo FAIL: t5_sample11 expected 0 V
end
meas tran t6_sample11 find v(t6) at=2199n
if abs(t6_sample11-(0)) > 0.5
let const.failures=const.failures+1
echo FAIL: t6_sample11 expected 0 V
end
meas tran a1_sample12 find v(a1) at=2399n
if abs(a1_sample12-(0)) > 0.5
let const.failures=const.failures+1
echo FAIL: a1_sample12 expected 0 V
end
meas tran a2_sample12 find v(a2) at=2399n
if abs(a2_sample12-(0)) > 0.5
let const.failures=const.failures+1
echo FAIL: a2_sample12 expected 0 V
end
meas tran a3_sample12 find v(a3) at=2399n
if abs(a3_sample12-(0)) > 0.5
let const.failures=const.failures+1
echo FAIL: a3_sample12 expected 0 V
end
meas tran a4_sample12 find v(a4) at=2399n
if abs(a4_sample12-(0)) > 0.5
let const.failures=const.failures+1
echo FAIL: a4_sample12 expected 0 V
end
meas tran a5_sample12 find v(a5) at=2399n
if abs(a5_sample12-(0)) > 0.5
let const.failures=const.failures+1
echo FAIL: a5_sample12 expected 0 V
end
meas tran a6_sample12 find v(a6) at=2399n
if abs(a6_sample12-(0)) > 0.5
let const.failures=const.failures+1
echo FAIL: a6_sample12 expected 0 V
end
meas tran b1_sample12 find v(b1) at=2399n
if abs(b1_sample12-(0)) > 0.5
let const.failures=const.failures+1
echo FAIL: b1_sample12 expected 0 V
end
meas tran b2_sample12 find v(b2) at=2399n
if abs(b2_sample12-(0)) > 0.5
let const.failures=const.failures+1
echo FAIL: b2_sample12 expected 0 V
end
meas tran b3_sample12 find v(b3) at=2399n
if abs(b3_sample12-(0)) > 0.5
let const.failures=const.failures+1
echo FAIL: b3_sample12 expected 0 V
end
meas tran b4_sample12 find v(b4) at=2399n
if abs(b4_sample12-(0)) > 0.5
let const.failures=const.failures+1
echo FAIL: b4_sample12 expected 0 V
end
meas tran b5_sample12 find v(b5) at=2399n
if abs(b5_sample12-(0)) > 0.5
let const.failures=const.failures+1
echo FAIL: b5_sample12 expected 0 V
end
meas tran b6_sample12 find v(b6) at=2399n
if abs(b6_sample12-(0)) > 0.5
let const.failures=const.failures+1
echo FAIL: b6_sample12 expected 0 V
end
meas tran t1_sample12 find v(t1) at=2399n
if abs(t1_sample12-(0)) > 0.5
let const.failures=const.failures+1
echo FAIL: t1_sample12 expected 0 V
end
meas tran t2_sample12 find v(t2) at=2399n
if abs(t2_sample12-(0)) > 0.5
let const.failures=const.failures+1
echo FAIL: t2_sample12 expected 0 V
end
meas tran t3_sample12 find v(t3) at=2399n
if abs(t3_sample12-(0)) > 0.5
let const.failures=const.failures+1
echo FAIL: t3_sample12 expected 0 V
end
meas tran t4_sample12 find v(t4) at=2399n
if abs(t4_sample12-(0)) > 0.5
let const.failures=const.failures+1
echo FAIL: t4_sample12 expected 0 V
end
meas tran t5_sample12 find v(t5) at=2399n
if abs(t5_sample12-(0)) > 0.5
let const.failures=const.failures+1
echo FAIL: t5_sample12 expected 0 V
end
meas tran t6_sample12 find v(t6) at=2399n
if abs(t6_sample12-(0)) > 0.5
let const.failures=const.failures+1
echo FAIL: t6_sample12 expected 0 V
end
meas tran a1_sample13 find v(a1) at=2599n
if abs(a1_sample13-(0)) > 0.5
let const.failures=const.failures+1
echo FAIL: a1_sample13 expected 0 V
end
meas tran a2_sample13 find v(a2) at=2599n
if abs(a2_sample13-(0)) > 0.5
let const.failures=const.failures+1
echo FAIL: a2_sample13 expected 0 V
end
meas tran a3_sample13 find v(a3) at=2599n
if abs(a3_sample13-(0)) > 0.5
let const.failures=const.failures+1
echo FAIL: a3_sample13 expected 0 V
end
meas tran a4_sample13 find v(a4) at=2599n
if abs(a4_sample13-(0)) > 0.5
let const.failures=const.failures+1
echo FAIL: a4_sample13 expected 0 V
end
meas tran a5_sample13 find v(a5) at=2599n
if abs(a5_sample13-(0)) > 0.5
let const.failures=const.failures+1
echo FAIL: a5_sample13 expected 0 V
end
meas tran a6_sample13 find v(a6) at=2599n
if abs(a6_sample13-(0)) > 0.5
let const.failures=const.failures+1
echo FAIL: a6_sample13 expected 0 V
end
meas tran b1_sample13 find v(b1) at=2599n
if abs(b1_sample13-(0)) > 0.5
let const.failures=const.failures+1
echo FAIL: b1_sample13 expected 0 V
end
meas tran b2_sample13 find v(b2) at=2599n
if abs(b2_sample13-(0)) > 0.5
let const.failures=const.failures+1
echo FAIL: b2_sample13 expected 0 V
end
meas tran b3_sample13 find v(b3) at=2599n
if abs(b3_sample13-(0)) > 0.5
let const.failures=const.failures+1
echo FAIL: b3_sample13 expected 0 V
end
meas tran b4_sample13 find v(b4) at=2599n
if abs(b4_sample13-(0)) > 0.5
let const.failures=const.failures+1
echo FAIL: b4_sample13 expected 0 V
end
meas tran b5_sample13 find v(b5) at=2599n
if abs(b5_sample13-(0)) > 0.5
let const.failures=const.failures+1
echo FAIL: b5_sample13 expected 0 V
end
meas tran b6_sample13 find v(b6) at=2599n
if abs(b6_sample13-(0)) > 0.5
let const.failures=const.failures+1
echo FAIL: b6_sample13 expected 0 V
end
meas tran t1_sample13 find v(t1) at=2599n
if abs(t1_sample13-(0)) > 0.5
let const.failures=const.failures+1
echo FAIL: t1_sample13 expected 0 V
end
meas tran t2_sample13 find v(t2) at=2599n
if abs(t2_sample13-(0)) > 0.5
let const.failures=const.failures+1
echo FAIL: t2_sample13 expected 0 V
end
meas tran t3_sample13 find v(t3) at=2599n
if abs(t3_sample13-(0)) > 0.5
let const.failures=const.failures+1
echo FAIL: t3_sample13 expected 0 V
end
meas tran t4_sample13 find v(t4) at=2599n
if abs(t4_sample13-(0)) > 0.5
let const.failures=const.failures+1
echo FAIL: t4_sample13 expected 0 V
end
meas tran t5_sample13 find v(t5) at=2599n
if abs(t5_sample13-(0)) > 0.5
let const.failures=const.failures+1
echo FAIL: t5_sample13 expected 0 V
end
meas tran t6_sample13 find v(t6) at=2599n
if abs(t6_sample13-(0)) > 0.5
let const.failures=const.failures+1
echo FAIL: t6_sample13 expected 0 V
end
meas tran a1_sample14 find v(a1) at=2799n
if abs(a1_sample14-(0)) > 0.5
let const.failures=const.failures+1
echo FAIL: a1_sample14 expected 0 V
end
meas tran a2_sample14 find v(a2) at=2799n
if abs(a2_sample14-(0)) > 0.5
let const.failures=const.failures+1
echo FAIL: a2_sample14 expected 0 V
end
meas tran a3_sample14 find v(a3) at=2799n
if abs(a3_sample14-(0)) > 0.5
let const.failures=const.failures+1
echo FAIL: a3_sample14 expected 0 V
end
meas tran a4_sample14 find v(a4) at=2799n
if abs(a4_sample14-(0)) > 0.5
let const.failures=const.failures+1
echo FAIL: a4_sample14 expected 0 V
end
meas tran a5_sample14 find v(a5) at=2799n
if abs(a5_sample14-(0)) > 0.5
let const.failures=const.failures+1
echo FAIL: a5_sample14 expected 0 V
end
meas tran a6_sample14 find v(a6) at=2799n
if abs(a6_sample14-(0)) > 0.5
let const.failures=const.failures+1
echo FAIL: a6_sample14 expected 0 V
end
meas tran b1_sample14 find v(b1) at=2799n
if abs(b1_sample14-(0)) > 0.5
let const.failures=const.failures+1
echo FAIL: b1_sample14 expected 0 V
end
meas tran b2_sample14 find v(b2) at=2799n
if abs(b2_sample14-(0)) > 0.5
let const.failures=const.failures+1
echo FAIL: b2_sample14 expected 0 V
end
meas tran b3_sample14 find v(b3) at=2799n
if abs(b3_sample14-(0)) > 0.5
let const.failures=const.failures+1
echo FAIL: b3_sample14 expected 0 V
end
meas tran b4_sample14 find v(b4) at=2799n
if abs(b4_sample14-(0)) > 0.5
let const.failures=const.failures+1
echo FAIL: b4_sample14 expected 0 V
end
meas tran b5_sample14 find v(b5) at=2799n
if abs(b5_sample14-(0)) > 0.5
let const.failures=const.failures+1
echo FAIL: b5_sample14 expected 0 V
end
meas tran b6_sample14 find v(b6) at=2799n
if abs(b6_sample14-(0)) > 0.5
let const.failures=const.failures+1
echo FAIL: b6_sample14 expected 0 V
end
meas tran t1_sample14 find v(t1) at=2799n
if abs(t1_sample14-(0)) > 0.5
let const.failures=const.failures+1
echo FAIL: t1_sample14 expected 0 V
end
meas tran t2_sample14 find v(t2) at=2799n
if abs(t2_sample14-(0)) > 0.5
let const.failures=const.failures+1
echo FAIL: t2_sample14 expected 0 V
end
meas tran t3_sample14 find v(t3) at=2799n
if abs(t3_sample14-(0)) > 0.5
let const.failures=const.failures+1
echo FAIL: t3_sample14 expected 0 V
end
meas tran t4_sample14 find v(t4) at=2799n
if abs(t4_sample14-(0)) > 0.5
let const.failures=const.failures+1
echo FAIL: t4_sample14 expected 0 V
end
meas tran t5_sample14 find v(t5) at=2799n
if abs(t5_sample14-(0)) > 0.5
let const.failures=const.failures+1
echo FAIL: t5_sample14 expected 0 V
end
meas tran t6_sample14 find v(t6) at=2799n
if abs(t6_sample14-(0)) > 0.5
let const.failures=const.failures+1
echo FAIL: t6_sample14 expected 0 V
end
meas tran a1_sample15 find v(a1) at=2999n
if abs(a1_sample15-(0)) > 0.5
let const.failures=const.failures+1
echo FAIL: a1_sample15 expected 0 V
end
meas tran a2_sample15 find v(a2) at=2999n
if abs(a2_sample15-(0)) > 0.5
let const.failures=const.failures+1
echo FAIL: a2_sample15 expected 0 V
end
meas tran a3_sample15 find v(a3) at=2999n
if abs(a3_sample15-(0)) > 0.5
let const.failures=const.failures+1
echo FAIL: a3_sample15 expected 0 V
end
meas tran a4_sample15 find v(a4) at=2999n
if abs(a4_sample15-(0)) > 0.5
let const.failures=const.failures+1
echo FAIL: a4_sample15 expected 0 V
end
meas tran a5_sample15 find v(a5) at=2999n
if abs(a5_sample15-(0)) > 0.5
let const.failures=const.failures+1
echo FAIL: a5_sample15 expected 0 V
end
meas tran a6_sample15 find v(a6) at=2999n
if abs(a6_sample15-(0)) > 0.5
let const.failures=const.failures+1
echo FAIL: a6_sample15 expected 0 V
end
meas tran b1_sample15 find v(b1) at=2999n
if abs(b1_sample15-(0)) > 0.5
let const.failures=const.failures+1
echo FAIL: b1_sample15 expected 0 V
end
meas tran b2_sample15 find v(b2) at=2999n
if abs(b2_sample15-(0)) > 0.5
let const.failures=const.failures+1
echo FAIL: b2_sample15 expected 0 V
end
meas tran b3_sample15 find v(b3) at=2999n
if abs(b3_sample15-(0)) > 0.5
let const.failures=const.failures+1
echo FAIL: b3_sample15 expected 0 V
end
meas tran b4_sample15 find v(b4) at=2999n
if abs(b4_sample15-(0)) > 0.5
let const.failures=const.failures+1
echo FAIL: b4_sample15 expected 0 V
end
meas tran b5_sample15 find v(b5) at=2999n
if abs(b5_sample15-(0)) > 0.5
let const.failures=const.failures+1
echo FAIL: b5_sample15 expected 0 V
end
meas tran b6_sample15 find v(b6) at=2999n
if abs(b6_sample15-(0)) > 0.5
let const.failures=const.failures+1
echo FAIL: b6_sample15 expected 0 V
end
meas tran t1_sample15 find v(t1) at=2999n
if abs(t1_sample15-(0)) > 0.5
let const.failures=const.failures+1
echo FAIL: t1_sample15 expected 0 V
end
meas tran t2_sample15 find v(t2) at=2999n
if abs(t2_sample15-(0)) > 0.5
let const.failures=const.failures+1
echo FAIL: t2_sample15 expected 0 V
end
meas tran t3_sample15 find v(t3) at=2999n
if abs(t3_sample15-(0)) > 0.5
let const.failures=const.failures+1
echo FAIL: t3_sample15 expected 0 V
end
meas tran t4_sample15 find v(t4) at=2999n
if abs(t4_sample15-(0)) > 0.5
let const.failures=const.failures+1
echo FAIL: t4_sample15 expected 0 V
end
meas tran t5_sample15 find v(t5) at=2999n
if abs(t5_sample15-(0)) > 0.5
let const.failures=const.failures+1
echo FAIL: t5_sample15 expected 0 V
end
meas tran t6_sample15 find v(t6) at=2999n
if abs(t6_sample15-(0)) > 0.5
let const.failures=const.failures+1
echo FAIL: t6_sample15 expected 0 V
end
if const.failures > 0
echo FAIL: NOR chain sampled logic errors
else
echo PASS: NOR chain all sampled stages within +/-0.5V
end
print const.failures
.endc

**** end user architecture code
**.ends

* expanding   symbol:  /home/ishi-kai/balanced-ternary-logic/nor.sym # of pins=5
** sym_path: member_project/balanced-ternary-logic/PenguinEino/nor.sym
** sch_path: member_project/balanced-ternary-logic/PenguinEino/nor.sch
.subckt nor a b vout V+ V-
*.iopin V+
*.ipin a
*.ipin b
*.opin vout
*.iopin V-
XXM4 net1 a V+ V+ PMOS w=46u l=1u nrd=0 nrs=0 m=1
XXM3 net2 b net1 V+ PMOS w=46u l=1u nrd=0 nrs=0 m=1
XR2 net2 vout V+ F_RR w=2.8e-06 l=17e-06 R=1 tc1=0 tc2=0 m=1
XR1 vout net3 V+ F_RR w=2.8e-06 l=17e-06 R=1 tc1=0 tc2=0 m=1
XXM2 net3 a V- V- NMOS w=6.5u l=1u nrd=0 nrs=0 m=1
XXM1 net3 b V- V- NMOS w=6.5u l=1u nrd=0 nrs=0 m=1
.ends

.GLOBAL GND
.end
